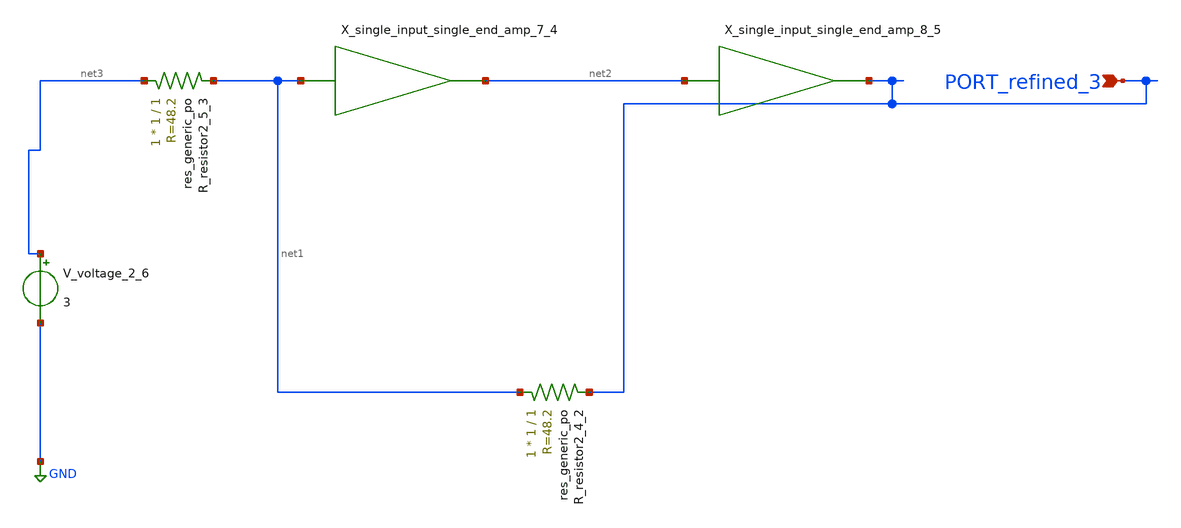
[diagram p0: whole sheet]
** sch_path: schematics/AMSNet/606.sch
**.subckt 606 PORT_refined_3
*.ipin PORT_refined_3
XR_resistor2_4_2 net1 PORT_refined_3 sky130_fd_pr__res_generic_po W=1 L=1 m=1
XR_resistor2_5_3 net3 net1 sky130_fd_pr__res_generic_po W=1 L=1 m=1
X_single_input_single_end_amp_7_4 net1 net2 schemgen_siso_amp
X_single_input_single_end_amp_8_5 net2 PORT_refined_3 schemgen_siso_amp
V_voltage_2_6 net3 GND 3
**.ends

* expanding   symbol:  schemgen_siso_amp.sym # of pins=2
** sym_path: symbols/schemgen_siso_amp.sym
.subckt schemgen_siso_amp IN OUT
* SchemGen ideal single-input amplifier: Vout = 1e5 * V(IN)
E1 OUT 0 IN 0 1e5
.ends schemgen_siso_amp
.GLOBAL GND
.end
